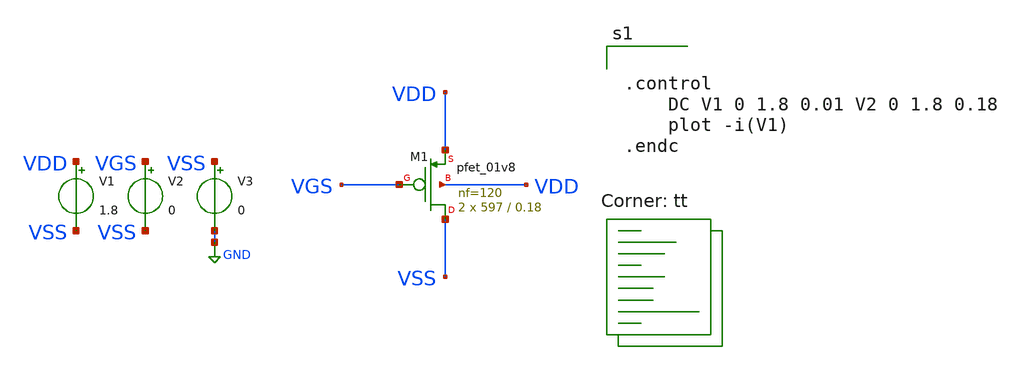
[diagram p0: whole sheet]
** sch_path: LDO_UVLO_Design/schematics/pass_element.sch
**.subckt pass_element
XM1 VSS VGS VDD VDD sky130_fd_pr__pfet_01v8 L=0.18 W=597 nf=120 ad='int((nf+1)/2) * W/nf * 0.29' as='int((nf+2)/2) * W/nf * 0.29'
+ pd='2*int((nf+1)/2) * (W/nf + 0.29)' ps='2*int((nf+2)/2) * (W/nf + 0.29)' nrd='0.29 / W' nrs='0.29 / W'
+ sa=0 sb=0 sd=0 mult=2 m=2
V1 VDD VSS 1.8
V2 VGS VSS 0
V3 VSS GND 0
**** begin user architecture code


.control
	DC V1 0 1.8 0.01 V2 0 1.8 0.18
	plot -i(V1)
.endc


.lib $::SKYWATER_MODELS/sky130.lib.spice tt
**** end user architecture code
**.ends
.GLOBAL GND
.end
